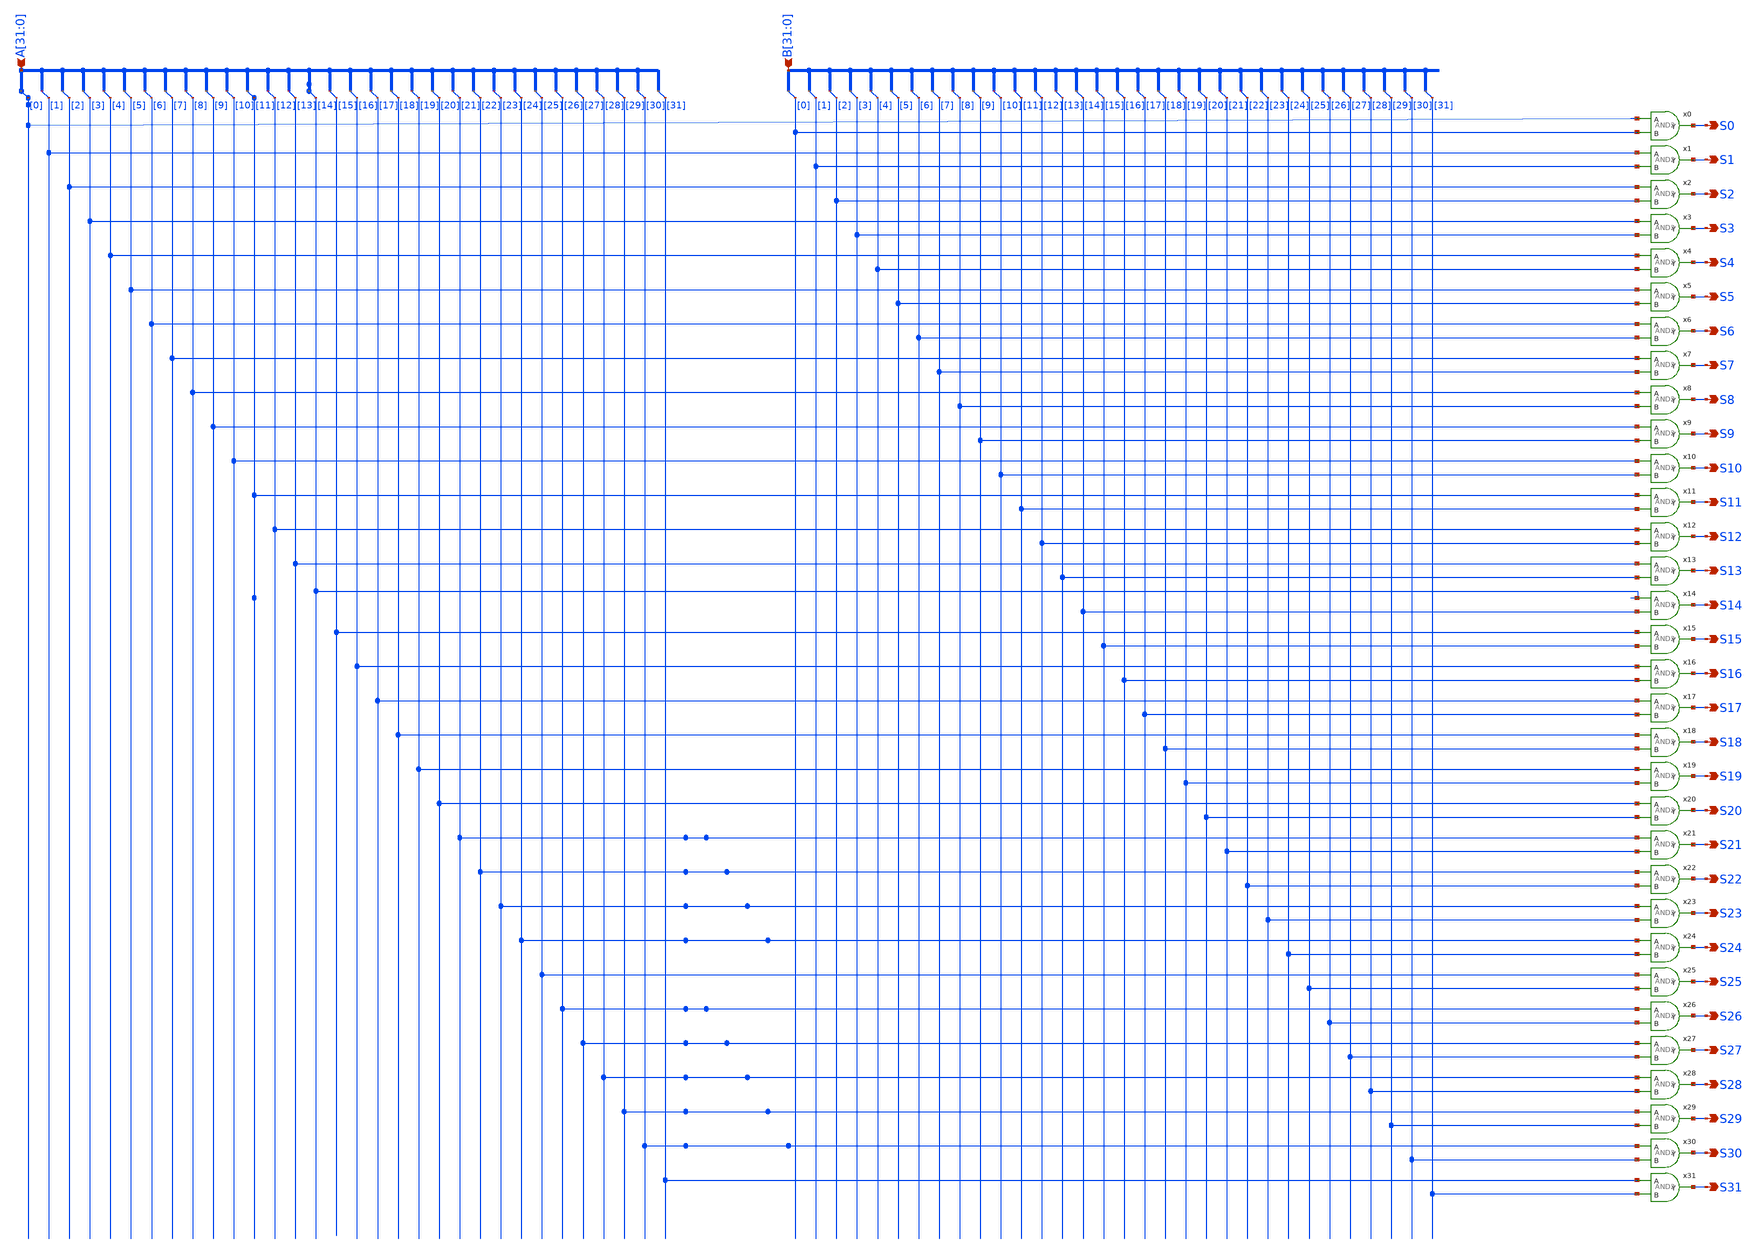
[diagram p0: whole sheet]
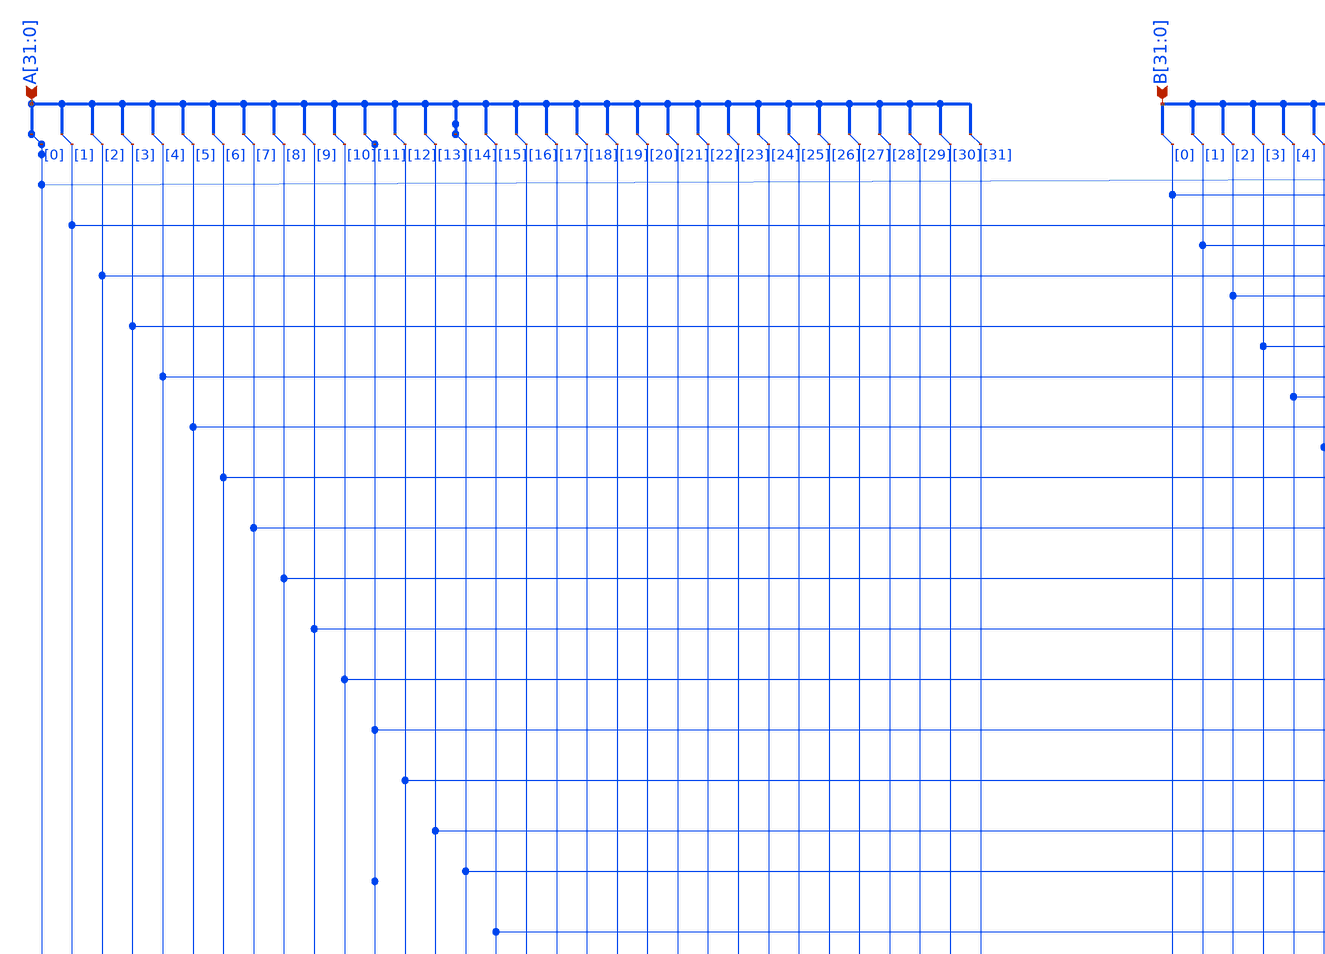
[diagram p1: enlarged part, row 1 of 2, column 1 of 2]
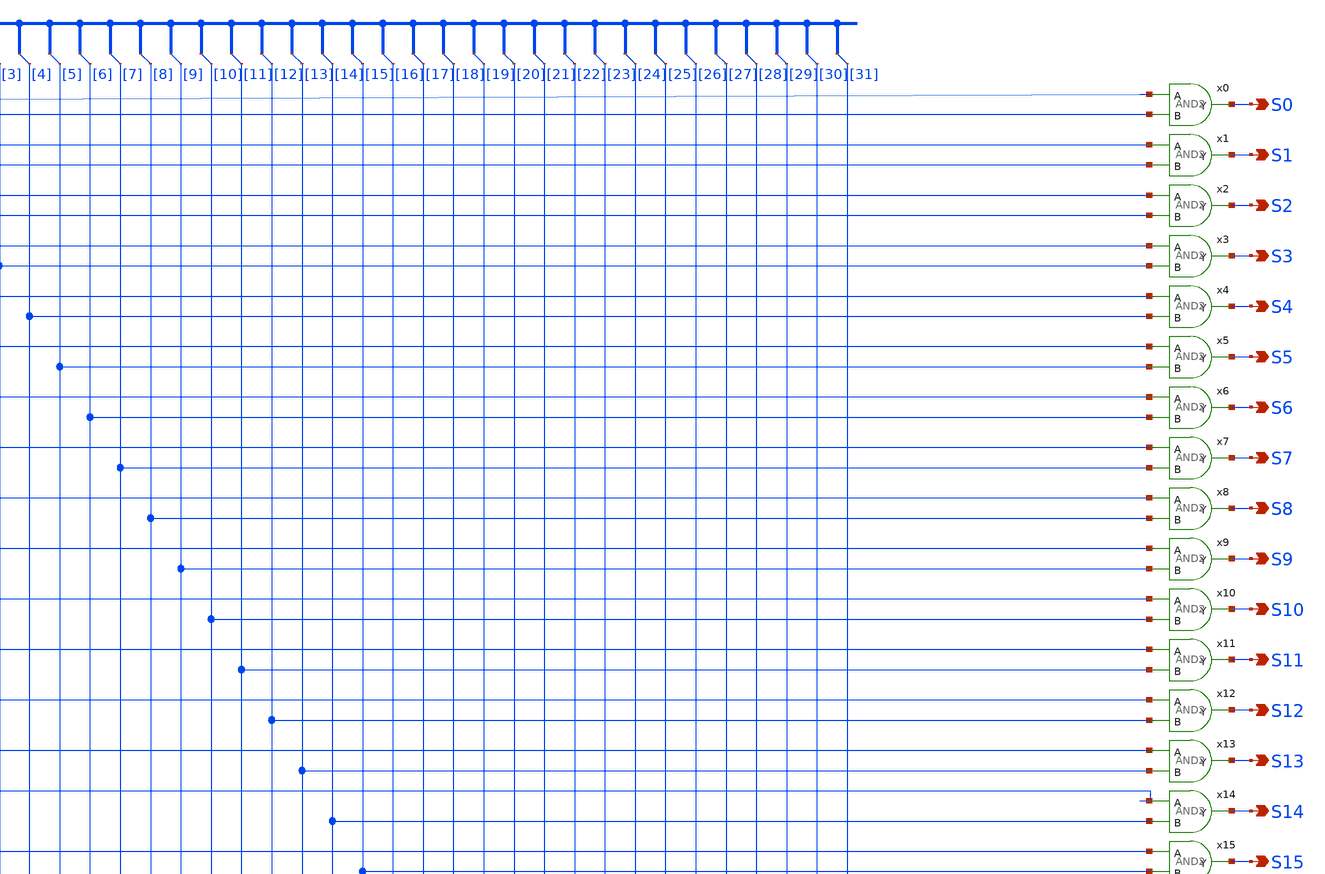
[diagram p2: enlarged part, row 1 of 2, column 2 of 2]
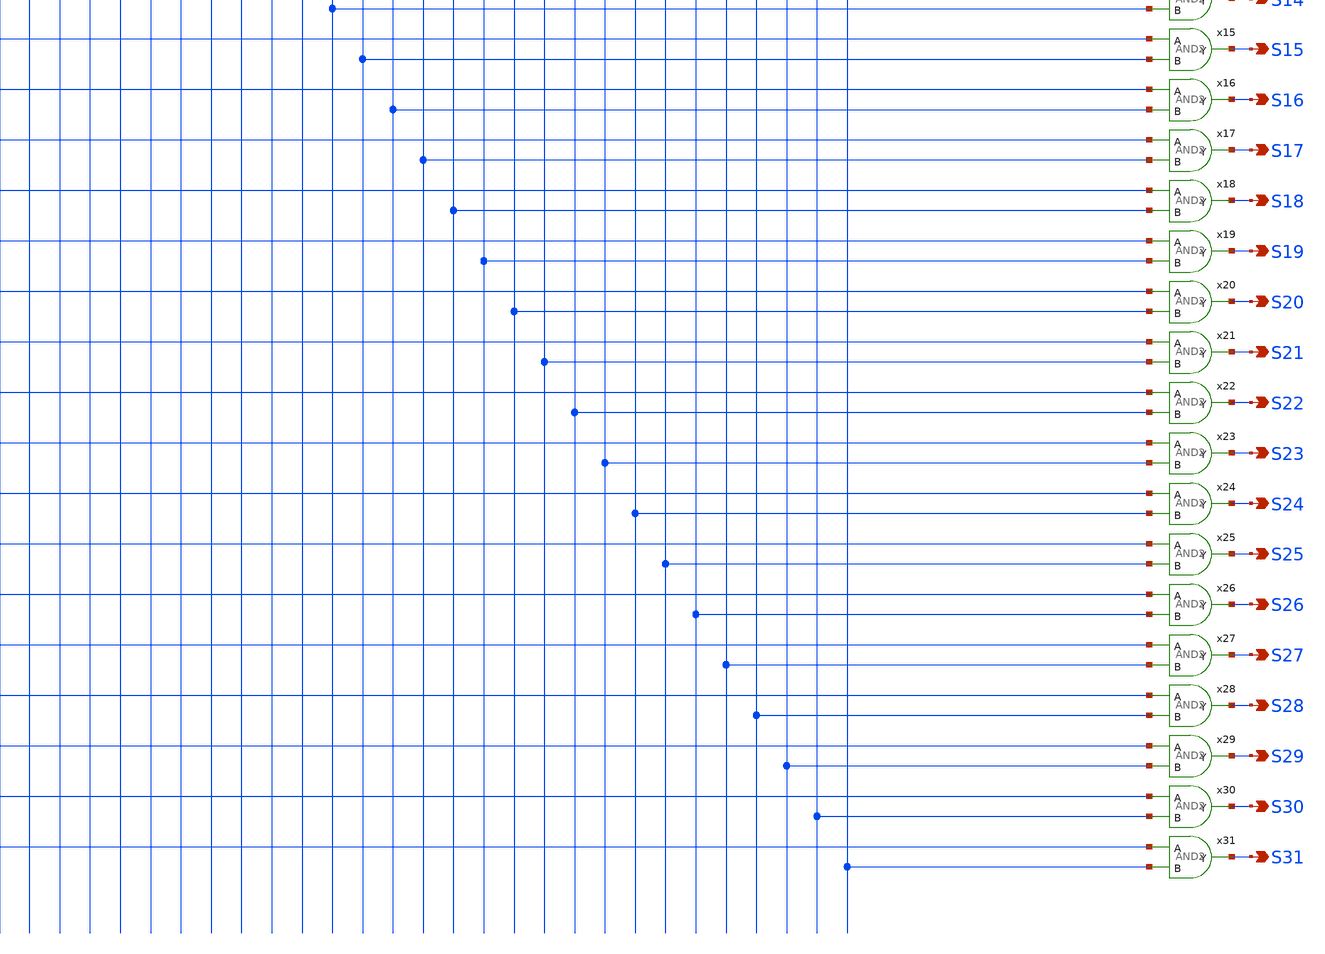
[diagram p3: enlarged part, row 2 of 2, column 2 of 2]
** sch_path: gates/32bit_AND.sch
**.subckt 32bit_AND S4 S5 S6 S7 S8 S9 S10 S11 S12 S13 S14 S15 S16 S17 S18 S19 S20 S21 S22 S23 S24
*+ S25 S26 S27 S28 S29 S30 S31 S0 S1 S2 S3
*+ A[31],A[30],A[29],A[28],A[27],A[26],A[25],A[24],A[23],A[22],A[21],A[20],A[19],A[18],A[17],A[16],A[15],A[14],A[13],A[12],A[11],A[10],A[9],A[8],A[7],A[6],A[5],A[4],A[3],A[2],A[1],A[0]
*+ B[31],B[30],B[29],B[28],B[27],B[26],B[25],B[24],B[23],B[22],B[21],B[20],B[19],B[18],B[17],B[16],B[15],B[14],B[13],B[12],B[11],B[10],B[9],B[8],B[7],B[6],B[5],B[4],B[3],B[2],B[1],B[0]
*.opin S4
*.opin S5
*.opin S6
*.opin S7
*.opin S8
*.opin S9
*.opin S10
*.opin S11
*.opin S12
*.opin S13
*.opin S14
*.opin S15
*.opin S16
*.opin S17
*.opin S18
*.opin S19
*.opin S20
*.opin S21
*.opin S22
*.opin S23
*.opin S24
*.opin S25
*.opin S26
*.opin S27
*.opin S28
*.opin S29
*.opin S30
*.opin S31
*.opin S0
*.opin S1
*.opin S2
*.opin S3
*.ipin
*+ A[31],A[30],A[29],A[28],A[27],A[26],A[25],A[24],A[23],A[22],A[21],A[20],A[19],A[18],A[17],A[16],A[15],A[14],A[13],A[12],A[11],A[10],A[9],A[8],A[7],A[6],A[5],A[4],A[3],A[2],A[1],A[0]
*.ipin
*+ B[31],B[30],B[29],B[28],B[27],B[26],B[25],B[24],B[23],B[22],B[21],B[20],B[19],B[18],B[17],B[16],B[15],B[14],B[13],B[12],B[11],B[10],B[9],B[8],B[7],B[6],B[5],B[4],B[3],B[2],B[1],B[0]
x0 A[0] S0 B[0] AND2
* tap: A[31:0] --> A[0]
* tap: A[31:0] --> A[1]
* tap: A[31:0] --> A[2]
* tap: A[31:0] --> A[3]
* tap: A[31:0] --> A[4]
* tap: A[31:0] --> A[5]
* tap: A[31:0] --> A[6]
* tap: A[31:0] --> A[7]
* tap: A[31:0] --> A[8]
* tap: A[31:0] --> A[9]
* tap: A[31:0] --> A[10]
* tap: A[31:0] --> A[11]
* tap: A[31:0] --> A[12]
* tap: A[31:0] --> A[13]
* tap: A[31:0] --> A[14]
* tap: A[31:0] --> A[15]
* tap: A[31:0] --> A[16]
* tap: A[31:0] --> A[17]
* tap: A[31:0] --> A[18]
* tap: A[31:0] --> A[19]
* tap: A[31:0] --> A[20]
* tap: A[31:0] --> A[21]
* tap: A[31:0] --> A[22]
* tap: A[31:0] --> A[23]
* tap: A[31:0] --> A[24]
* tap: A[31:0] --> A[25]
* tap: A[31:0] --> A[26]
* tap: A[31:0] --> A[27]
* tap: A[31:0] --> A[28]
* tap: A[31:0] --> A[29]
* tap: A[31:0] --> A[30]
* tap: A[31:0] --> A[31]
* tap: B[31:0] --> B[0]
* tap: B[31:0] --> B[1]
* tap: B[31:0] --> B[2]
* tap: B[31:0] --> B[3]
* tap: B[31:0] --> B[4]
* tap: B[31:0] --> B[5]
* tap: B[31:0] --> B[6]
* tap: B[31:0] --> B[7]
* tap: B[31:0] --> B[8]
* tap: B[31:0] --> B[9]
* tap: B[31:0] --> B[10]
* tap: B[31:0] --> B[11]
* tap: B[31:0] --> B[12]
* tap: B[31:0] --> B[13]
* tap: B[31:0] --> B[14]
* tap: B[31:0] --> B[15]
* tap: B[31:0] --> B[16]
* tap: B[31:0] --> B[17]
* tap: B[31:0] --> B[18]
* tap: B[31:0] --> B[19]
* tap: B[31:0] --> B[20]
* tap: B[31:0] --> B[21]
* tap: B[31:0] --> B[22]
* tap: B[31:0] --> B[23]
* tap: B[31:0] --> B[24]
* tap: B[31:0] --> B[25]
* tap: B[31:0] --> B[26]
* tap: B[31:0] --> B[27]
* tap: B[31:0] --> B[28]
* tap: B[31:0] --> B[29]
* tap: B[31:0] --> B[30]
* tap: B[31:0] --> B[31]
x1 A[1] S1 B[1] AND2
x2 A[2] S2 B[2] AND2
x3 A[3] S3 B[3] AND2
x4 A[4] S4 B[4] AND2
x5 A[5] S5 B[5] AND2
x6 A[6] S6 B[6] AND2
x8 A[8] S8 B[8] AND2
x9 A[9] S9 B[9] AND2
x10 A[10] S10 B[10] AND2
x11 A[11] S11 B[11] AND2
x12 A[12] S12 B[12] AND2
x13 A[13] S13 B[13] AND2
x14 A[14] S14 B[14] AND2
x15 A[15] S15 B[15] AND2
x16 A[16] S16 B[16] AND2
x17 A[17] S17 B[17] AND2
x18 A[18] S18 B[18] AND2
x19 A[19] S19 B[19] AND2
x20 A[20] S20 B[20] AND2
x21 A[21] S21 B[21] AND2
x22 A[22] S22 B[22] AND2
x23 A[23] S23 B[23] AND2
x24 A[24] S24 B[24] AND2
x25 A[25] S25 B[25] AND2
x26 A[26] S26 B[26] AND2
x27 A[27] S27 B[27] AND2
x28 A[28] S28 B[28] AND2
x29 A[29] S29 B[29] AND2
x30 A[30] S30 B[30] AND2
x31 A[31] S31 B[31] AND2
x7 A[7] S7 B[7] AND2
**.ends

* expanding   symbol:  AND2.sym # of pins=3
** sym_path: gates/AND2.sym
** sch_path: gates/AND2.sch
.subckt AND2 A Y B
*.opin Y
*.ipin A
*.ipin B
x1 A net1 B NAND2_Gate
X2 net1 Y inv_vtc
.ends


* expanding   symbol:  NAND2_Gate.sym # of pins=3
** sym_path: gates/NAND2_Gate.sym
** sch_path: gates/NAND2_Gate.sch
.subckt NAND2_Gate A Y B
*.ipin A
*.ipin B
*.opin Y
XM1 Y A net1 GND sky130_fd_pr__nfet_01v8 L=0.15 W=1 nf=1 ad='int((nf+1)/2) * W/nf * 0.29' as='int((nf+2)/2) * W/nf * 0.29'
+ pd='2*int((nf+1)/2) * (W/nf + 0.29)' ps='2*int((nf+2)/2) * (W/nf + 0.29)' nrd='0.29 / W' nrs='0.29 / W'
+ sa=0 sb=0 sd=0 mult=1 m=1
XM2 net1 B GND GND sky130_fd_pr__nfet_01v8 L=0.15 W=1 nf=1 ad='int((nf+1)/2) * W/nf * 0.29' as='int((nf+2)/2) * W/nf * 0.29'
+ pd='2*int((nf+1)/2) * (W/nf + 0.29)' ps='2*int((nf+2)/2) * (W/nf + 0.29)' nrd='0.29 / W' nrs='0.29 / W'
+ sa=0 sb=0 sd=0 mult=1 m=1
XM3 Y A VDD VDD sky130_fd_pr__pfet_01v8 L=0.15 W=1 nf=1 ad='int((nf+1)/2) * W/nf * 0.29' as='int((nf+2)/2) * W/nf * 0.29'
+ pd='2*int((nf+1)/2) * (W/nf + 0.29)' ps='2*int((nf+2)/2) * (W/nf + 0.29)' nrd='0.29 / W' nrs='0.29 / W'
+ sa=0 sb=0 sd=0 mult=1 m=1
XM4 Y B VDD VDD sky130_fd_pr__pfet_01v8 L=0.15 W=1 nf=1 ad='int((nf+1)/2) * W/nf * 0.29' as='int((nf+2)/2) * W/nf * 0.29'
+ pd='2*int((nf+1)/2) * (W/nf + 0.29)' ps='2*int((nf+2)/2) * (W/nf + 0.29)' nrd='0.29 / W' nrs='0.29 / W'
+ sa=0 sb=0 sd=0 mult=1 m=1
.ends


* expanding   symbol:  /home/apn/test_xschem_sky130/inv_vtc.sym # of pins=2
** sym_path: gates/inv_vtc.sym
** sch_path: gates/inv_vtc.sch
.subckt inv_vtc A Y
*.ipin A
*.opin Y
XM1 Y A VDD VDD sky130_fd_pr__pfet_01v8 L=0.15 W=2 nf=1 ad='int((nf+1)/2) * W/nf * 0.29' as='int((nf+2)/2) * W/nf * 0.29'
+ pd='2*int((nf+1)/2) * (W/nf + 0.29)' ps='2*int((nf+2)/2) * (W/nf + 0.29)' nrd='0.29 / W' nrs='0.29 / W'
+ sa=0 sb=0 sd=0 mult=1 m=1
XM2 Y A GND GND sky130_fd_pr__nfet_01v8 L=0.15 W=1 nf=1 ad='int((nf+1)/2) * W/nf * 0.29' as='int((nf+2)/2) * W/nf * 0.29'
+ pd='2*int((nf+1)/2) * (W/nf + 0.29)' ps='2*int((nf+2)/2) * (W/nf + 0.29)' nrd='0.29 / W' nrs='0.29 / W'
+ sa=0 sb=0 sd=0 mult=1 m=1
.ends

.GLOBAL VDD
.GLOBAL GND
.end
